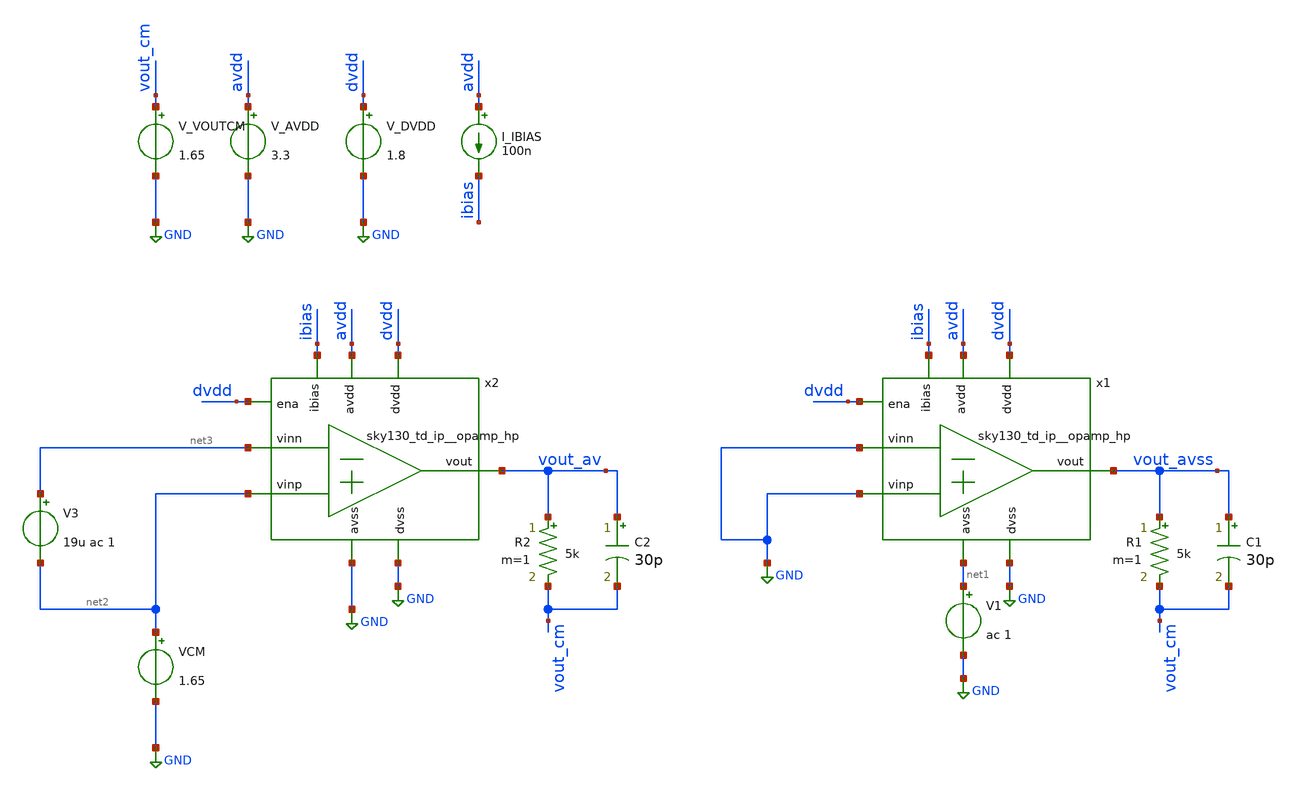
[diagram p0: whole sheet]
** sch_path: xschem/psrrn.sch
**.subckt psrrn
x1 avdd vout_avss ibias GND GND net1 dvdd GND dvdd sky130_td_ip__opamp_hp
V_AVDD avdd GND 3.3
.save i(v_avdd)
V_DVDD dvdd GND 1.8
.save i(v_dvdd)
I_IBIAS avdd ibias 100n
R1 vout_avss vout_cm 5k m=1
C1 vout_avss vout_cm 30p m=1
V_VOUTCM vout_cm GND 1.65
.save i(v_voutcm)
V1 net1 GND ac 1
x2 avdd vout_av ibias net3 net2 GND dvdd GND dvdd sky130_td_ip__opamp_hp
R2 vout_av vout_cm 5k m=1
C2 vout_av vout_cm 30p m=1
V3 net3 net2 19u ac 1
VCM net2 GND 1.65
.save i(vcm)
**** begin user architecture code


.save all

.control
save all

* Run AC sweep from 1Hz to 1GHz
AC DEC 100 1 1000000000
run

* Get DC gain in DBs.
let av_db = db(vout_av)
let avss_db = db(vout_avss)
let psrrn_db = av_db - avss_db

meas AC psrrn_dc FIND psrrn_db AT=1
meas AC psrrn_100k FIND psrrn_db AT=100K

echo
echo ===================================
echo PSRR- characterization results:
echo - PSRR @ 1 Hz: $&psrrn_dc
echo - PSRR @ 100 kHz: $&psrrn_100k
echo ===================================


plot psrrn_db

.endc




.lib /usr/local/share/pdk/sky130A/libs.tech/combined/sky130.lib.spice tt


**** end user architecture code
**.ends
.GLOBAL GND
.end
